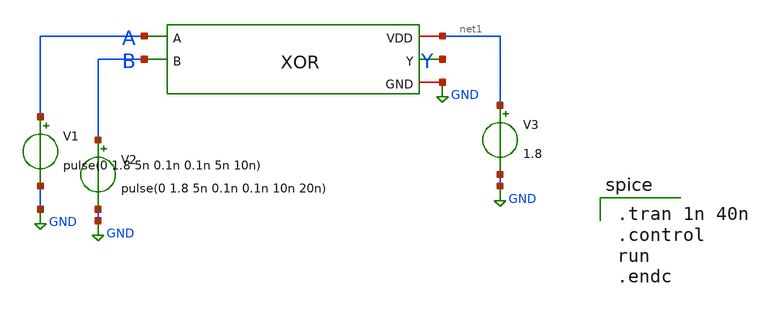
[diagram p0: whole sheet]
** sch_path: XOR/XOR_Testbench.sch
**.subckt XOR_Testbench
x1 net1 A Y B GND XOR
V1 A GND pulse(0 1.8 5n 0.1n 0.1n 5n 10n)
V2 B GND pulse(0 1.8 5n 0.1n 0.1n 10n 20n)
V3 net1 GND 1.8
**** begin user architecture code

.lib /usr/local/share/pdk/sky130A/libs.tech/ngspice/sky130.lib.spice tt


.tran 1n 40n
.control
run
.endc

**** end user architecture code
**.ends

* expanding   symbol:  /home/ee431/workspace/XOR/XOR.sym # of pins=5
** sym_path: XOR/XOR.sym
** sch_path: XOR/XOR.sch
.subckt XOR VDD A Y B GND
*.ipin A
*.ipin B
*.opin Y
*.iopin GND
*.iopin VDD
XM1 Y A net2 GND sky130_fd_pr__nfet_01v8 L=0.5 W=2 nf=1 ad='int((nf+1)/2) * W/nf * 0.29' as='int((nf+2)/2) * W/nf * 0.29'
+ pd='2*int((nf+1)/2) * (W/nf + 0.29)' ps='2*int((nf+2)/2) * (W/nf + 0.29)' nrd='0.29 / W' nrs='0.29 / W'
+ sa=0 sb=0 sd=0 mult=1 m=1
XM2 Y net3 net1 GND sky130_fd_pr__nfet_01v8 L=0.5 W=2 nf=1 ad='int((nf+1)/2) * W/nf * 0.29' as='int((nf+2)/2) * W/nf * 0.29'
+ pd='2*int((nf+1)/2) * (W/nf + 0.29)' ps='2*int((nf+2)/2) * (W/nf + 0.29)' nrd='0.29 / W' nrs='0.29 / W'
+ sa=0 sb=0 sd=0 mult=1 m=1
XM3 net2 B GND GND sky130_fd_pr__nfet_01v8 L=0.5 W=2 nf=1 ad='int((nf+1)/2) * W/nf * 0.29' as='int((nf+2)/2) * W/nf * 0.29'
+ pd='2*int((nf+1)/2) * (W/nf + 0.29)' ps='2*int((nf+2)/2) * (W/nf + 0.29)' nrd='0.29 / W' nrs='0.29 / W'
+ sa=0 sb=0 sd=0 mult=1 m=1
XM4 net1 net4 GND GND sky130_fd_pr__nfet_01v8 L=0.5 W=2 nf=1 ad='int((nf+1)/2) * W/nf * 0.29' as='int((nf+2)/2) * W/nf * 0.29'
+ pd='2*int((nf+1)/2) * (W/nf + 0.29)' ps='2*int((nf+2)/2) * (W/nf + 0.29)' nrd='0.29 / W' nrs='0.29 / W'
+ sa=0 sb=0 sd=0 mult=1 m=1
XM5 Y net3 net5 VDD sky130_fd_pr__pfet_01v8 L=0.5 W=4 nf=1 ad='int((nf+1)/2) * W/nf * 0.29' as='int((nf+2)/2) * W/nf * 0.29'
+ pd='2*int((nf+1)/2) * (W/nf + 0.29)' ps='2*int((nf+2)/2) * (W/nf + 0.29)' nrd='0.29 / W' nrs='0.29 / W'
+ sa=0 sb=0 sd=0 mult=1 m=1
XM6 Y A net2 GND sky130_fd_pr__nfet_01v8 L=0.15 W=1 nf=1 ad='int((nf+1)/2) * W/nf * 0.29' as='int((nf+2)/2) * W/nf * 0.29'
+ pd='2*int((nf+1)/2) * (W/nf + 0.29)' ps='2*int((nf+2)/2) * (W/nf + 0.29)' nrd='0.29 / W' nrs='0.29 / W'
+ sa=0 sb=0 sd=0 mult=1 m=1
XM7 Y net4 net5 VDD sky130_fd_pr__pfet_01v8 L=0.5 W=4 nf=1 ad='int((nf+1)/2) * W/nf * 0.29' as='int((nf+2)/2) * W/nf * 0.29'
+ pd='2*int((nf+1)/2) * (W/nf + 0.29)' ps='2*int((nf+2)/2) * (W/nf + 0.29)' nrd='0.29 / W' nrs='0.29 / W'
+ sa=0 sb=0 sd=0 mult=1 m=1
XM8 net5 A VDD VDD sky130_fd_pr__pfet_01v8 L=0.5 W=4 nf=1 ad='int((nf+1)/2) * W/nf * 0.29' as='int((nf+2)/2) * W/nf * 0.29'
+ pd='2*int((nf+1)/2) * (W/nf + 0.29)' ps='2*int((nf+2)/2) * (W/nf + 0.29)' nrd='0.29 / W' nrs='0.29 / W'
+ sa=0 sb=0 sd=0 mult=1 m=1
XM9 net5 B VDD VDD sky130_fd_pr__pfet_01v8 L=0.5 W=4 nf=1 ad='int((nf+1)/2) * W/nf * 0.29' as='int((nf+2)/2) * W/nf * 0.29'
+ pd='2*int((nf+1)/2) * (W/nf + 0.29)' ps='2*int((nf+2)/2) * (W/nf + 0.29)' nrd='0.29 / W' nrs='0.29 / W'
+ sa=0 sb=0 sd=0 mult=1 m=1
x1 VDD A net3 GND Inverter
x2 VDD B net4 GND Inverter
.ends


* expanding   symbol:  /home/ee431/workspace/inverter/Inverter.sym # of pins=4
** sym_path: inverter/Inverter.sym
** sch_path: inverter/Inverter.sch
.subckt Inverter VDD A Y GND
*.ipin A
*.opin Y
*.iopin VDD
*.iopin GND
XM1 Y A VDD VDD sky130_fd_pr__pfet_01v8 L=0.5 W=2 nf=1 ad='int((nf+1)/2) * W/nf * 0.29' as='int((nf+2)/2) * W/nf * 0.29'
+ pd='2*int((nf+1)/2) * (W/nf + 0.29)' ps='2*int((nf+2)/2) * (W/nf + 0.29)' nrd='0.29 / W' nrs='0.29 / W'
+ sa=0 sb=0 sd=0 mult=1 m=1
XM2 Y A GND GND sky130_fd_pr__nfet_01v8 L=0.5 W=1 nf=1 ad='int((nf+1)/2) * W/nf * 0.29' as='int((nf+2)/2) * W/nf * 0.29'
+ pd='2*int((nf+1)/2) * (W/nf + 0.29)' ps='2*int((nf+2)/2) * (W/nf + 0.29)' nrd='0.29 / W' nrs='0.29 / W'
+ sa=0 sb=0 sd=0 mult=1 m=1
.ends

.GLOBAL GND
.end
